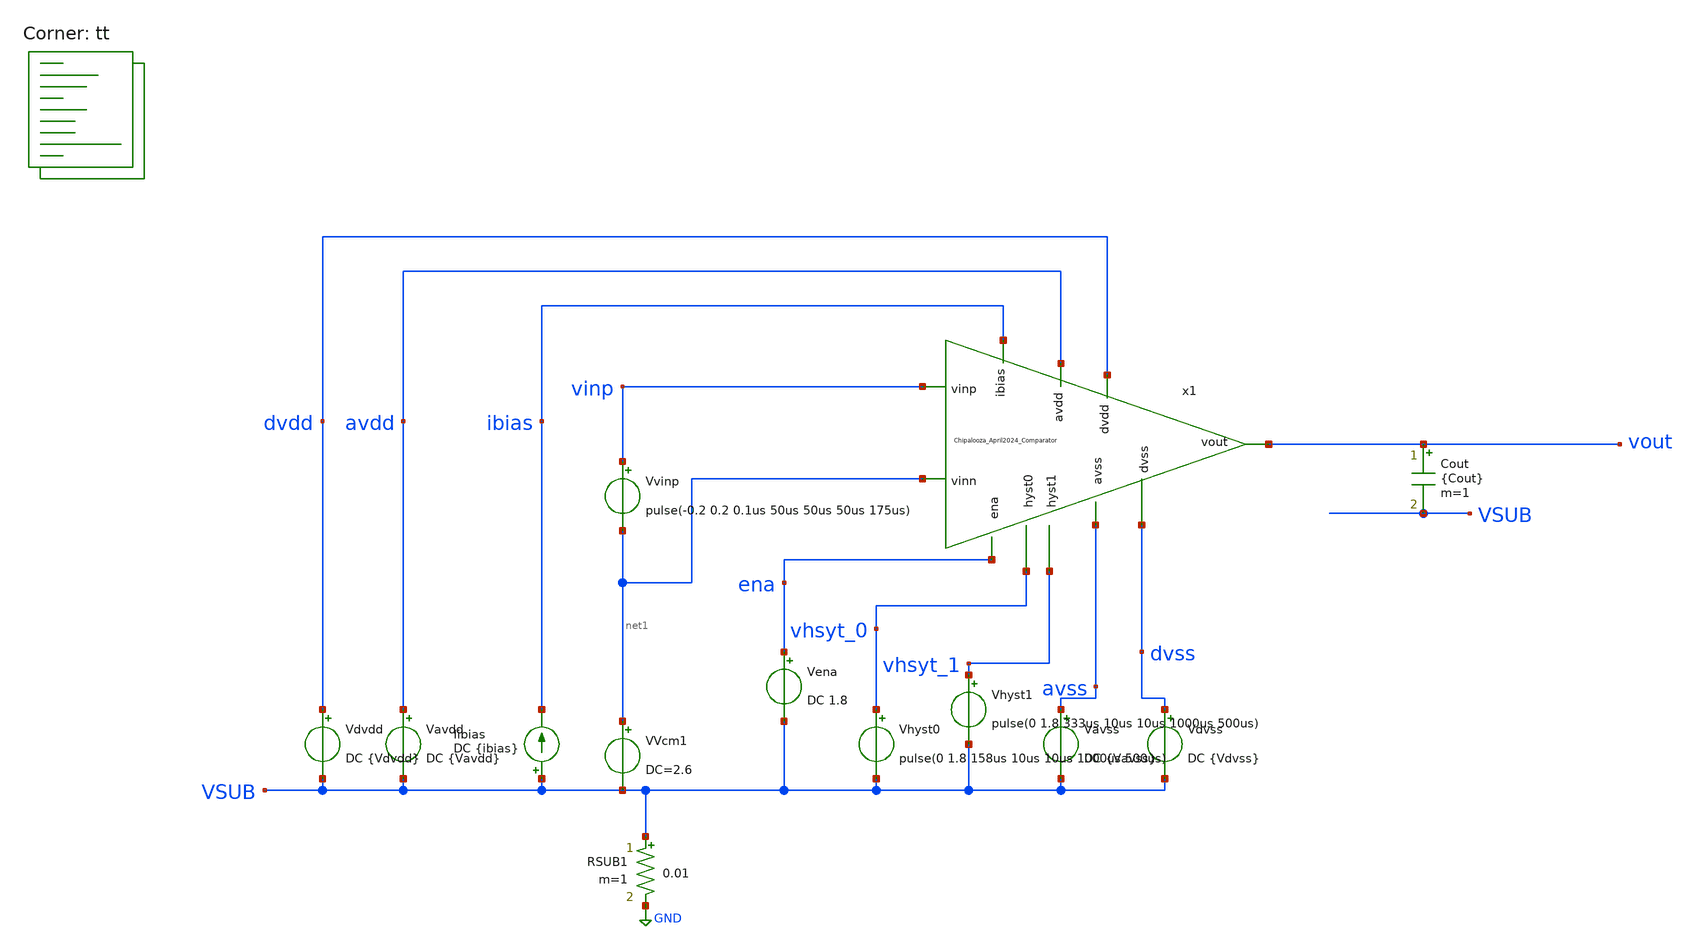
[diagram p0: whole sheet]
** sch_path: Chipalooza_April2024_Comparator/xschem/TB_hysteresis.sch
**.subckt TB_hysteresis
Vavdd avdd VSUB DC {Vavdd}
Cout vout VSUB {Cout} m=1
Vdvdd dvdd VSUB DC {Vdvdd}
Vena ena VSUB DC 1.8
Vhyst0 vhsyt_0 VSUB pulse(0 1.8 158us 10us 10us 1000us 500us)
Vhyst1 vhsyt_1 VSUB pulse(0 1.8 333us 10us 10us 1000us 500us)
Vavss avss VSUB DC {Vavss}
Vdvss dvss VSUB DC {Vdvss}
Iibias VSUB ibias DC {ibias}
RSUB1 VSUB GND 0.01 m=1
VVcm1 net1 VSUB DC=2.6
Vvinp vinp net1 pulse(-0.2 0.2 0.1us 50us 50us 50us 175us)
x1 vhsyt_0 vhsyt_1 avdd vinp avss net1 dvdd dvss vout ibias ena Chipalooza_April2024_Comparator
**** begin user architecture code
.lib $::SKYWATER_MODELS/sky130.lib.spice tt

* this option enables mos model bin
* selection based on W/NF instead of W
*.option wnflag=1
.option savecurrents
.option save all

.control

.param vdvdd=1.8 vavdd=3.3 cout=1f
.param ibias=1u ena=1 Vhyst_0=1 Vhyst_1=1
.param vavss=0 vdvss=0
.param Vcm=0

*dc VVcm 0 3.3 0.1
*plot v(vout) v(inx)

tran 0.01u 525u
*plot v(vout) v(vinp)

meas tran tr1 TRIG AT=0u TARG v(vout) VAL=1.79 RISE=1
meas tran vin_tr1 find v(vinp) at=tr1

meas tran tf1 TRIG AT=0u TARG v(vout) VAL=0.01 FALL=1
meas tran vin_tf1 find v(vinp) at=tf1

meas tran tr2 TRIG AT=0u TARG v(vout) VAL=1.79 RISE=2
meas tran vin_tr2 find v(vinp) at=tr1

meas tran tf2 TRIG AT=0u TARG v(vout) VAL=0.01 FALL=2
meas tran vin_tf2 find v(vinp) at=tf2

meas tran tr3 TRIG AT=0u TARG v(vout) VAL=1.79 RISE=3
meas tran vin_tr3 find v(vinp) at=tr3

meas tran tf3 TRIG AT=0u TARG v(vout) VAL=0.01 FALL=3
meas tran vin_tf3 find v(vinp) at=tf3

let hyst1=(vin_tf1-vin_tr1)
let hyst2=(vin_tf2-vin_tr2)
let hyst3=(vin_tf3-vin_tr3)

print hyst1
print hyst2
print hyst3

write TB_hysteresis.raw


*quit 0

.endc


**** end user architecture code
**.ends

* expanding   symbol:  Chipalooza_April2024_Comparator.sym # of pins=11
** sym_path: Chipalooza_April2024_Comparator/xschem/Chipalooza_April2024_Comparator.sym
** sch_path: Chipalooza_April2024_Comparator/xschem/Chipalooza_April2024_Comparator.sch
.subckt Chipalooza_April2024_Comparator hyst0 hyst1 avdd vinp avss vinn dvdd dvss vout ibias ena
*.ipin vinp
*.ipin vinn
*.ipin hyst0
*.ipin hyst1
*.ipin avdd
*.ipin avss
*.ipin dvdd
*.ipin dvss
*.opin vout
*.ipin ena
*.ipin ibias
XM16 dvdd hyst1 net1 dvss sky130_fd_pr__nfet_01v8 L=0.15 W=16 nf=1 ad='int((1 + 1)/2) * 16 / 1 * 0.29'
+ as='int((1 + 2)/2) * 16 / 1 * 0.29' pd='2*int((1 + 1)/2) * (16 / 1 + 0.29)' ps='2*int((1 + 2)/2) * (16 / 1 + 0.29)'
+ nrd='0.29 / 16 ' nrs='0.29 / 16 ' sa=0 sb=0 sd=0 mult=8 m=8
XM19 net1 hyst_bias0 I_hyst dvss sky130_fd_pr__nfet_01v8 L=0.15 W=16 nf=1 ad='int((1 + 1)/2) * 16 / 1 * 0.29'
+ as='int((1 + 2)/2) * 16 / 1 * 0.29' pd='2*int((1 + 1)/2) * (16 / 1 + 0.29)' ps='2*int((1 + 2)/2) * (16 / 1 + 0.29)'
+ nrd='0.29 / 16 ' nrs='0.29 / 16 ' sa=0 sb=0 sd=0 mult=8 m=8
V4 Pbias avss 2.5
V5 Nbias avss 3
XM29 SumOutBar SumOut dvdd dvdd sky130_fd_pr__pfet_01v8 L=1 W=2 nf=1 ad='int((nf+1)/2) * W/nf * 0.29'
+ as='int((nf+2)/2) * W/nf * 0.29' pd='2*int((nf+1)/2) * (W/nf + 0.29)' ps='2*int((nf+2)/2) * (W/nf + 0.29)'
+ nrd='0.29 / W' nrs='0.29 / W' sa=0 sb=0 sd=0 mult=2 m=2
XM30 SumOutBar SumOut dvss dvss sky130_fd_pr__nfet_01v8 L=1 W=1 nf=1 ad='int((nf+1)/2) * W/nf * 0.29'
+ as='int((nf+2)/2) * W/nf * 0.29' pd='2*int((nf+1)/2) * (W/nf + 0.29)' ps='2*int((nf+2)/2) * (W/nf + 0.29)'
+ nrd='0.29 / W' nrs='0.29 / W' sa=0 sb=0 sd=0 mult=2 m=2
XM31 vout SumOutBar dvdd dvdd sky130_fd_pr__pfet_01v8 L=0.15 W=1 nf=1 ad='int((nf+1)/2) * W/nf * 0.29'
+ as='int((nf+2)/2) * W/nf * 0.29' pd='2*int((nf+1)/2) * (W/nf + 0.29)' ps='2*int((nf+2)/2) * (W/nf + 0.29)'
+ nrd='0.29 / W' nrs='0.29 / W' sa=0 sb=0 sd=0 mult=1 m=1
XM32 vout SumOutBar dvss dvss sky130_fd_pr__nfet_01v8 L=0.15 W=1 nf=1 ad='int((nf+1)/2) * W/nf * 0.29'
+ as='int((nf+2)/2) * W/nf * 0.29' pd='2*int((nf+1)/2) * (W/nf + 0.29)' ps='2*int((nf+2)/2) * (W/nf + 0.29)'
+ nrd='0.29 / W' nrs='0.29 / W' sa=0 sb=0 sd=0 mult=1 m=1
XM4 net3 net3 avdd avdd sky130_fd_pr__pfet_g5v0d10v5 L=1 W=2 nf=1 ad='int((nf+1)/2) * W/nf * 0.29' as='int((nf+2)/2) * W/nf * 0.29'
+ pd='2*int((nf+1)/2) * (W/nf + 0.29)' ps='2*int((nf+2)/2) * (W/nf + 0.29)' nrd='0.29 / W' nrs='0.29 / W'
+ sa=0 sb=0 sd=0 mult=2 m=2
XM5 N1 net3 avdd avdd sky130_fd_pr__pfet_g5v0d10v5 L=1 W=2 nf=1 ad='int((nf+1)/2) * W/nf * 0.29' as='int((nf+2)/2) * W/nf * 0.29'
+ pd='2*int((nf+1)/2) * (W/nf + 0.29)' ps='2*int((nf+2)/2) * (W/nf + 0.29)' nrd='0.29 / W' nrs='0.29 / W'
+ sa=0 sb=0 sd=0 mult=2 m=2
XM6 N2 net3 avdd avdd sky130_fd_pr__pfet_g5v0d10v5 L=1 W=2 nf=1 ad='int((nf+1)/2) * W/nf * 0.29' as='int((nf+2)/2) * W/nf * 0.29'
+ pd='2*int((nf+1)/2) * (W/nf + 0.29)' ps='2*int((nf+2)/2) * (W/nf + 0.29)' nrd='0.29 / W' nrs='0.29 / W'
+ sa=0 sb=0 sd=0 mult=2 m=2
XM7 SumOut Bias1 N2 avdd sky130_fd_pr__pfet_g5v0d10v5 L=1 W=2 nf=1 ad='int((nf+1)/2) * W/nf * 0.29' as='int((nf+2)/2) * W/nf * 0.29'
+ pd='2*int((nf+1)/2) * (W/nf + 0.29)' ps='2*int((nf+2)/2) * (W/nf + 0.29)' nrd='0.29 / W' nrs='0.29 / W'
+ sa=0 sb=0 sd=0 mult=2 m=2
XM8 Sum Bias1 N1 avdd sky130_fd_pr__pfet_g5v0d10v5 L=1 W=2 nf=1 ad='int((nf+1)/2) * W/nf * 0.29' as='int((nf+2)/2) * W/nf * 0.29'
+ pd='2*int((nf+1)/2) * (W/nf + 0.29)' ps='2*int((nf+2)/2) * (W/nf + 0.29)' nrd='0.29 / W' nrs='0.29 / W'
+ sa=0 sb=0 sd=0 mult=2 m=2
XM9 SumOut Bias2 P2 avss sky130_fd_pr__nfet_g5v0d10v5 L=1 W=2 nf=1 ad='int((nf+1)/2) * W/nf * 0.29' as='int((nf+2)/2) * W/nf * 0.29'
+ pd='2*int((nf+1)/2) * (W/nf + 0.29)' ps='2*int((nf+2)/2) * (W/nf + 0.29)' nrd='0.29 / W' nrs='0.29 / W'
+ sa=0 sb=0 sd=0 mult=2 m=2
XM10 Sum Bias2 P1 avss sky130_fd_pr__nfet_g5v0d10v5 L=1 W=2 nf=1 ad='int((nf+1)/2) * W/nf * 0.29' as='int((nf+2)/2) * W/nf * 0.29'
+ pd='2*int((nf+1)/2) * (W/nf + 0.29)' ps='2*int((nf+2)/2) * (W/nf + 0.29)' nrd='0.29 / W' nrs='0.29 / W'
+ sa=0 sb=0 sd=0 mult=2 m=2
XM11 P2 Sum avss avss sky130_fd_pr__nfet_g5v0d10v5 L=1 W=2 nf=1 ad='int((nf+1)/2) * W/nf * 0.29' as='int((nf+2)/2) * W/nf * 0.29'
+ pd='2*int((nf+1)/2) * (W/nf + 0.29)' ps='2*int((nf+2)/2) * (W/nf + 0.29)' nrd='0.29 / W' nrs='0.29 / W'
+ sa=0 sb=0 sd=0 mult=2 m=2
XM12 P1 Sum avss avss sky130_fd_pr__nfet_g5v0d10v5 L=1 W=2 nf=1 ad='int((nf+1)/2) * W/nf * 0.29' as='int((nf+2)/2) * W/nf * 0.29'
+ pd='2*int((nf+1)/2) * (W/nf + 0.29)' ps='2*int((nf+2)/2) * (W/nf + 0.29)' nrd='0.29 / W' nrs='0.29 / W'
+ sa=0 sb=0 sd=0 mult=2 m=2
I1 net3 net9 1u
C38 avss 0 2p m=1
XM24 net5 ena avss avss sky130_fd_pr__nfet_g5v0d10v5 L=1 W=16 nf=1 ad='int((nf+1)/2) * W/nf * 0.29' as='int((nf+2)/2) * W/nf * 0.29'
+ pd='2*int((nf+1)/2) * (W/nf + 0.29)' ps='2*int((nf+2)/2) * (W/nf + 0.29)' nrd='0.29 / W' nrs='0.29 / W'
+ sa=0 sb=0 sd=0 mult=2 m=2
XM1 P2 vinn psource_input avdd sky130_fd_pr__pfet_g5v0d10v5 L=1 W=2 nf=1 ad='int((nf+1)/2) * W/nf * 0.29'
+ as='int((nf+2)/2) * W/nf * 0.29' pd='2*int((nf+1)/2) * (W/nf + 0.29)' ps='2*int((nf+2)/2) * (W/nf + 0.29)'
+ nrd='0.29 / W' nrs='0.29 / W' sa=0 sb=0 sd=0 mult=2 m=2
XM2 P1 vinp psource_input avdd sky130_fd_pr__pfet_g5v0d10v5 L=1 W=2 nf=1 ad='int((nf+1)/2) * W/nf * 0.29'
+ as='int((nf+2)/2) * W/nf * 0.29' pd='2*int((nf+1)/2) * (W/nf + 0.29)' ps='2*int((nf+2)/2) * (W/nf + 0.29)'
+ nrd='0.29 / W' nrs='0.29 / W' sa=0 sb=0 sd=0 mult=2 m=2
XM3 psource_input net4 avdd avdd sky130_fd_pr__pfet_g5v0d10v5 L=1 W=3 nf=1 ad='int((nf+1)/2) * W/nf * 0.29'
+ as='int((nf+2)/2) * W/nf * 0.29' pd='2*int((nf+1)/2) * (W/nf + 0.29)' ps='2*int((nf+2)/2) * (W/nf + 0.29)'
+ nrd='0.29 / W' nrs='0.29 / W' sa=0 sb=0 sd=0 mult=4 m=4
XM14 net4 net4 avdd avdd sky130_fd_pr__pfet_g5v0d10v5 L=1 W=2 nf=1 ad='int((nf+1)/2) * W/nf * 0.29' as='int((nf+2)/2) * W/nf * 0.29'
+ pd='2*int((nf+1)/2) * (W/nf + 0.29)' ps='2*int((nf+2)/2) * (W/nf + 0.29)' nrd='0.29 / W' nrs='0.29 / W'
+ sa=0 sb=0 sd=0 mult=2 m=2
XM15 nbias_tail Pbias psource_input avdd sky130_fd_pr__pfet_g5v0d10v5 L=1 W=2 nf=1 ad='int((nf+1)/2) * W/nf * 0.29'
+ as='int((nf+2)/2) * W/nf * 0.29' pd='2*int((nf+1)/2) * (W/nf + 0.29)' ps='2*int((nf+2)/2) * (W/nf + 0.29)'
+ nrd='0.29 / W' nrs='0.29 / W' sa=0 sb=0 sd=0 mult=2 m=2
XM17 N1 vinp ndrain_input avss sky130_fd_pr__nfet_g5v0d10v5 L=1 W=1 nf=1 ad='int((nf+1)/2) * W/nf * 0.29'
+ as='int((nf+2)/2) * W/nf * 0.29' pd='2*int((nf+1)/2) * (W/nf + 0.29)' ps='2*int((nf+2)/2) * (W/nf + 0.29)'
+ nrd='0.29 / W' nrs='0.29 / W' sa=0 sb=0 sd=0 mult=2 m=2
XM20 N2 vinn ndrain_input avss sky130_fd_pr__nfet_g5v0d10v5 L=1 W=1 nf=1 ad='int((nf+1)/2) * W/nf * 0.29'
+ as='int((nf+2)/2) * W/nf * 0.29' pd='2*int((nf+1)/2) * (W/nf + 0.29)' ps='2*int((nf+2)/2) * (W/nf + 0.29)'
+ nrd='0.29 / W' nrs='0.29 / W' sa=0 sb=0 sd=0 mult=2 m=2
XM21 ndrain_input nbias_tail net5 avss sky130_fd_pr__nfet_g5v0d10v5 L=1 W=4 nf=1 ad='int((nf+1)/2) * W/nf * 0.29'
+ as='int((nf+2)/2) * W/nf * 0.29' pd='2*int((nf+1)/2) * (W/nf + 0.29)' ps='2*int((nf+2)/2) * (W/nf + 0.29)'
+ nrd='0.29 / W' nrs='0.29 / W' sa=0 sb=0 sd=0 mult=2 m=2
XM22 nbias_tail nbias_tail net5 avss sky130_fd_pr__nfet_g5v0d10v5 L=1 W=2 nf=1 ad='int((nf+1)/2) * W/nf * 0.29'
+ as='int((nf+2)/2) * W/nf * 0.29' pd='2*int((nf+1)/2) * (W/nf + 0.29)' ps='2*int((nf+2)/2) * (W/nf + 0.29)'
+ nrd='0.29 / W' nrs='0.29 / W' sa=0 sb=0 sd=0 mult=2 m=2
XM23 net4 Nbias ndrain_input avss sky130_fd_pr__nfet_g5v0d10v5 L=1 W=2 nf=1 ad='int((nf+1)/2) * W/nf * 0.29'
+ as='int((nf+2)/2) * W/nf * 0.29' pd='2*int((nf+1)/2) * (W/nf + 0.29)' ps='2*int((nf+2)/2) * (W/nf + 0.29)'
+ nrd='0.29 / W' nrs='0.29 / W' sa=0 sb=0 sd=0 mult=2 m=2
XM25 net6 I_hyst avss avss sky130_fd_pr__nfet_g5v0d10v5 L=1 W=2 nf=1 ad='int((nf+1)/2) * W/nf * 0.29'
+ as='int((nf+2)/2) * W/nf * 0.29' pd='2*int((nf+1)/2) * (W/nf + 0.29)' ps='2*int((nf+2)/2) * (W/nf + 0.29)'
+ nrd='0.29 / W' nrs='0.29 / W' sa=0 sb=0 sd=0 mult=2 m=2
XMHyst I_hyst I_hyst avss avss sky130_fd_pr__nfet_g5v0d10v5 L=1 W=8 nf=1 ad='int((nf+1)/2) * W/nf * 0.29'
+ as='int((nf+2)/2) * W/nf * 0.29' pd='2*int((nf+1)/2) * (W/nf + 0.29)' ps='2*int((nf+2)/2) * (W/nf + 0.29)'
+ nrd='0.29 / W' nrs='0.29 / W' sa=0 sb=0 sd=0 mult=2 m=2
XM28 avss SumOutBar net6 avss sky130_fd_pr__nfet_g5v0d10v5 L=1 W=2 nf=1 ad='int((nf+1)/2) * W/nf * 0.29'
+ as='int((nf+2)/2) * W/nf * 0.29' pd='2*int((nf+1)/2) * (W/nf + 0.29)' ps='2*int((nf+2)/2) * (W/nf + 0.29)'
+ nrd='0.29 / W' nrs='0.29 / W' sa=0 sb=0 sd=0 mult=2 m=2
XM33 avss SumOut net6 avss sky130_fd_pr__nfet_g5v0d10v5 L=1 W=2 nf=1 ad='int((nf+1)/2) * W/nf * 0.29'
+ as='int((nf+2)/2) * W/nf * 0.29' pd='2*int((nf+1)/2) * (W/nf + 0.29)' ps='2*int((nf+2)/2) * (W/nf + 0.29)'
+ nrd='0.29 / W' nrs='0.29 / W' sa=0 sb=0 sd=0 mult=2 m=2
XM26 hyst_bias0 ibias dvss dvss sky130_fd_pr__nfet_01v8 L=0.15 W=16 nf=1 ad='int((1 + 1)/2) * 16 / 1 * 0.29'
+ as='int((1 + 2)/2) * 16 / 1 * 0.29' pd='2*int((1 + 1)/2) * (16 / 1 + 0.29)' ps='2*int((1 + 2)/2) * (16 / 1 + 0.29)'
+ nrd='0.29 / 16 ' nrs='0.29 / 16 ' sa=0 sb=0 sd=0 mult=8 m=8
XM27 ibias ibias dvss dvss sky130_fd_pr__nfet_01v8 L=0.15 W=16 nf=1 ad='int((1 + 1)/2) * 16 / 1 * 0.29'
+ as='int((1 + 2)/2) * 16 / 1 * 0.29' pd='2*int((1 + 1)/2) * (16 / 1 + 0.29)' ps='2*int((1 + 2)/2) * (16 / 1 + 0.29)'
+ nrd='0.29 / 16 ' nrs='0.29 / 16 ' sa=0 sb=0 sd=0 mult=8 m=8
XM34 hyst_bias1 hyst_bias0 dvdd dvdd sky130_fd_pr__pfet_01v8 L=0.15 W=16 nf=1 ad='int((nf+1)/2) * W/nf * 0.29'
+ as='int((nf+2)/2) * W/nf * 0.29' pd='2*int((nf+1)/2) * (W/nf + 0.29)' ps='2*int((nf+2)/2) * (W/nf + 0.29)'
+ nrd='0.29 / W' nrs='0.29 / W' sa=0 sb=0 sd=0 mult=8 m=8
XM35 hyst_bias0 hyst_bias0 dvdd dvdd sky130_fd_pr__pfet_01v8 L=0.15 W=16 nf=1 ad='int((nf+1)/2) * W/nf * 0.29'
+ as='int((nf+2)/2) * W/nf * 0.29' pd='2*int((nf+1)/2) * (W/nf + 0.29)' ps='2*int((nf+2)/2) * (W/nf + 0.29)'
+ nrd='0.29 / W' nrs='0.29 / W' sa=0 sb=0 sd=0 mult=8 m=8
XM36 dvdd hyst_bias1 dvss dvss sky130_fd_pr__nfet_01v8 L=0.15 W=16 nf=1 ad='int((1 + 1)/2) * 16 / 1 * 0.29'
+ as='int((1 + 2)/2) * 16 / 1 * 0.29' pd='2*int((1 + 1)/2) * (16 / 1 + 0.29)' ps='2*int((1 + 2)/2) * (16 / 1 + 0.29)'
+ nrd='0.29 / 16 ' nrs='0.29 / 16 ' sa=0 sb=0 sd=0 mult=8 m=8
XM37 hyst_bias1 hyst_bias1 dvss dvss sky130_fd_pr__nfet_01v8 L=0.15 W=16 nf=1 ad='int((1 + 1)/2) * 16 / 1 * 0.29'
+ as='int((1 + 2)/2) * 16 / 1 * 0.29' pd='2*int((1 + 1)/2) * (16 / 1 + 0.29)' ps='2*int((1 + 2)/2) * (16 / 1 + 0.29)'
+ nrd='0.29 / 16 ' nrs='0.29 / 16 ' sa=0 sb=0 sd=0 mult=8 m=8
XM13 dvdd hyst0 net2 dvss sky130_fd_pr__nfet_01v8 L=0.15 W=2 nf=1 ad='int((1 + 1)/2) * 2 / 1 * 0.29'
+ as='int((1 + 2)/2) * 2 / 1 * 0.29' pd='2*int((1 + 1)/2) * (2 / 1 + 0.29)' ps='2*int((1 + 2)/2) * (2 / 1 + 0.29)'
+ nrd='0.29 / 2 ' nrs='0.29 / 2 ' sa=0 sb=0 sd=0 mult=2 m=2
XM18 net2 hyst_bias0 I_hyst dvss sky130_fd_pr__nfet_01v8 L=0.15 W=2 nf=1 ad='int((1 + 1)/2) * 2 / 1 * 0.29'
+ as='int((1 + 2)/2) * 2 / 1 * 0.29' pd='2*int((1 + 1)/2) * (2 / 1 + 0.29)' ps='2*int((1 + 2)/2) * (2 / 1 + 0.29)'
+ nrd='0.29 / 2 ' nrs='0.29 / 2 ' sa=0 sb=0 sd=0 mult=2 m=2
V2 Bias1 avss 2.5
V1 Bias2 avss 2.5
XM39 net7 I_hyst avss avss sky130_fd_pr__nfet_g5v0d10v5 L=1 W=2 nf=1 ad='int((nf+1)/2) * W/nf * 0.29'
+ as='int((nf+2)/2) * W/nf * 0.29' pd='2*int((nf+1)/2) * (W/nf + 0.29)' ps='2*int((nf+2)/2) * (W/nf + 0.29)'
+ nrd='0.29 / W' nrs='0.29 / W' sa=0 sb=0 sd=0 mult=2 m=2
XMHyst1 I_hyst I_hyst avss avss sky130_fd_pr__nfet_g5v0d10v5 L=1 W=2 nf=1 ad='int((nf+1)/2) * W/nf * 0.29'
+ as='int((nf+2)/2) * W/nf * 0.29' pd='2*int((nf+1)/2) * (W/nf + 0.29)' ps='2*int((nf+2)/2) * (W/nf + 0.29)'
+ nrd='0.29 / W' nrs='0.29 / W' sa=0 sb=0 sd=0 mult=2 m=2
XM41 avdd SumOut net8 avdd sky130_fd_pr__pfet_g5v0d10v5 L=1 W=2 nf=1 ad='int((nf+1)/2) * W/nf * 0.29'
+ as='int((nf+2)/2) * W/nf * 0.29' pd='2*int((nf+1)/2) * (W/nf + 0.29)' ps='2*int((nf+2)/2) * (W/nf + 0.29)'
+ nrd='0.29 / W' nrs='0.29 / W' sa=0 sb=0 sd=0 mult=2 m=2
XM40 net10 SumOutBar net11 avdd sky130_fd_pr__pfet_g5v0d10v5 L=1 W=2 nf=1 ad='int((nf+1)/2) * W/nf * 0.29'
+ as='int((nf+2)/2) * W/nf * 0.29' pd='2*int((nf+1)/2) * (W/nf + 0.29)' ps='2*int((nf+2)/2) * (W/nf + 0.29)'
+ nrd='0.29 / W' nrs='0.29 / W' sa=0 sb=0 sd=0 mult=2 m=2
XM42 net7 net7 avdd avdd sky130_fd_pr__pfet_g5v0d10v5 L=1 W=2 nf=1 ad='int((nf+1)/2) * W/nf * 0.29' as='int((nf+2)/2) * W/nf * 0.29'
+ pd='2*int((nf+1)/2) * (W/nf + 0.29)' ps='2*int((nf+2)/2) * (W/nf + 0.29)' nrd='0.29 / W' nrs='0.29 / W'
+ sa=0 sb=0 sd=0 mult=2 m=2
XM43 net8 net7 avdd avdd sky130_fd_pr__pfet_01v8 L=0.15 W=2 nf=1 ad='int((nf+1)/2) * W/nf * 0.29' as='int((nf+2)/2) * W/nf * 0.29'
+ pd='2*int((nf+1)/2) * (W/nf + 0.29)' ps='2*int((nf+2)/2) * (W/nf + 0.29)' nrd='0.29 / W' nrs='0.29 / W'
+ sa=0 sb=0 sd=0 mult=2 m=2
I2 avdd psource_input 1u
I3 ndrain_input avss 1u
.ends

.GLOBAL GND
.end
